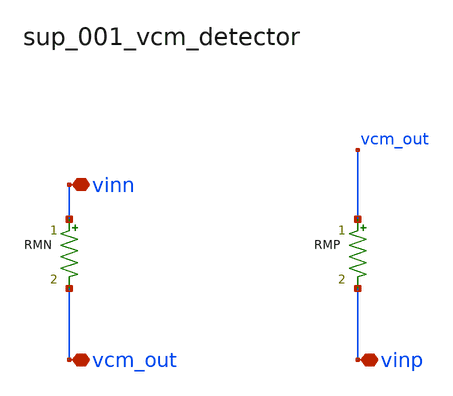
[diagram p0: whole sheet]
** sch_path: analog-db/raw/sup_001_vcm_detector/sup_001_vcm_detector_annotated.sch
**.subckt sup_001_vcm_detector_annotated vinn vcm_out vinp
*.iopin vinn
*.iopin vcm_out
*.iopin vinp
RMN vinn vcm_out 'x_dut_rmn_value' m=1
RMP vcm_out vinp 'x_dut_rmp_value' m=1
**.ends
.end
